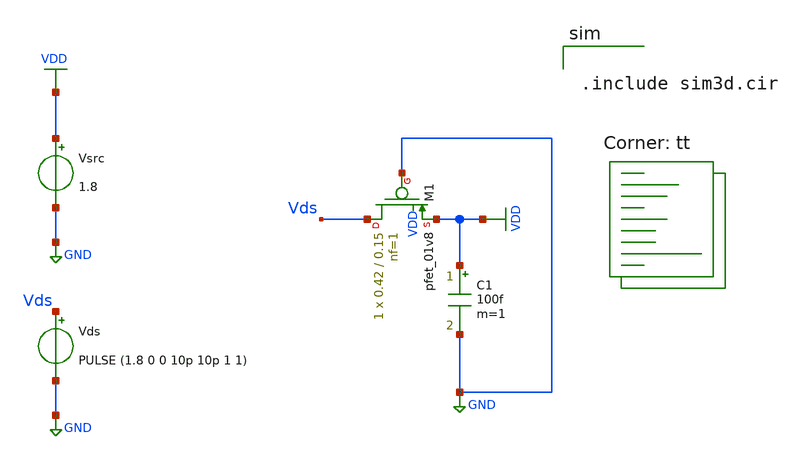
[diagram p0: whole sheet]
** sch_path: assignments/assignment1/assign3d.sch
**.subckt assign3d
XM1 Vds GND VDD VDD sky130_fd_pr__pfet_01v8 L=0.15 W=0.42 nf=1 ad='int((nf+1)/2) * W/nf * 0.29' as='int((nf+2)/2) * W/nf * 0.29'
+ pd='2*int((nf+1)/2) * (W/nf + 0.29)' ps='2*int((nf+2)/2) * (W/nf + 0.29)' nrd='0.29 / W' nrs='0.29 / W'
+ sa=0 sb=0 sd=0 mult=1 m=1
Vsrc VDD GND 1.8
Vds Vds GND PULSE (1.8 0 0 10p 10p 1 1)
C1 VDD GND 100f m=1
**** begin user architecture code


.include sim3d.cir


.lib $::SKYWATER_MODELS/sky130.lib.spice tt
**** end user architecture code
**.ends
.GLOBAL VDD
.GLOBAL GND
.end
